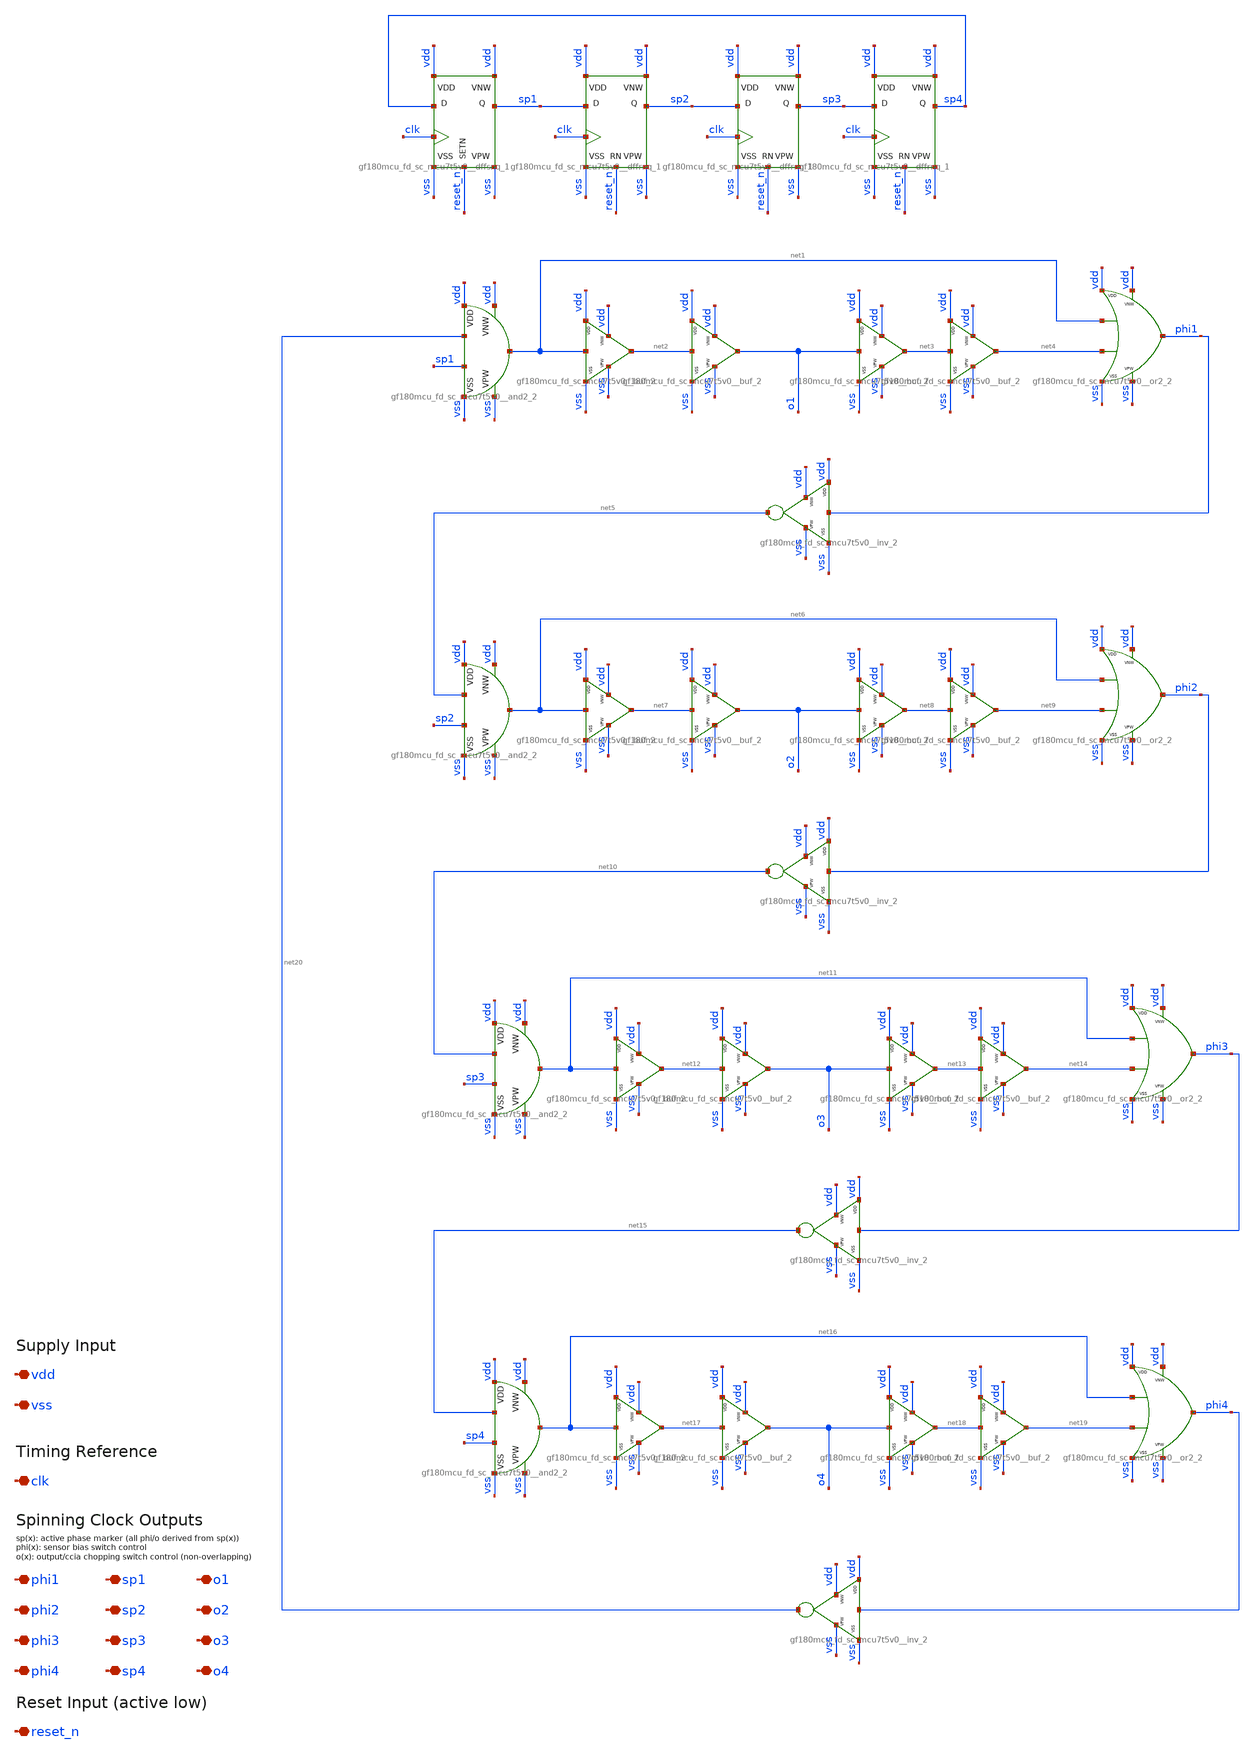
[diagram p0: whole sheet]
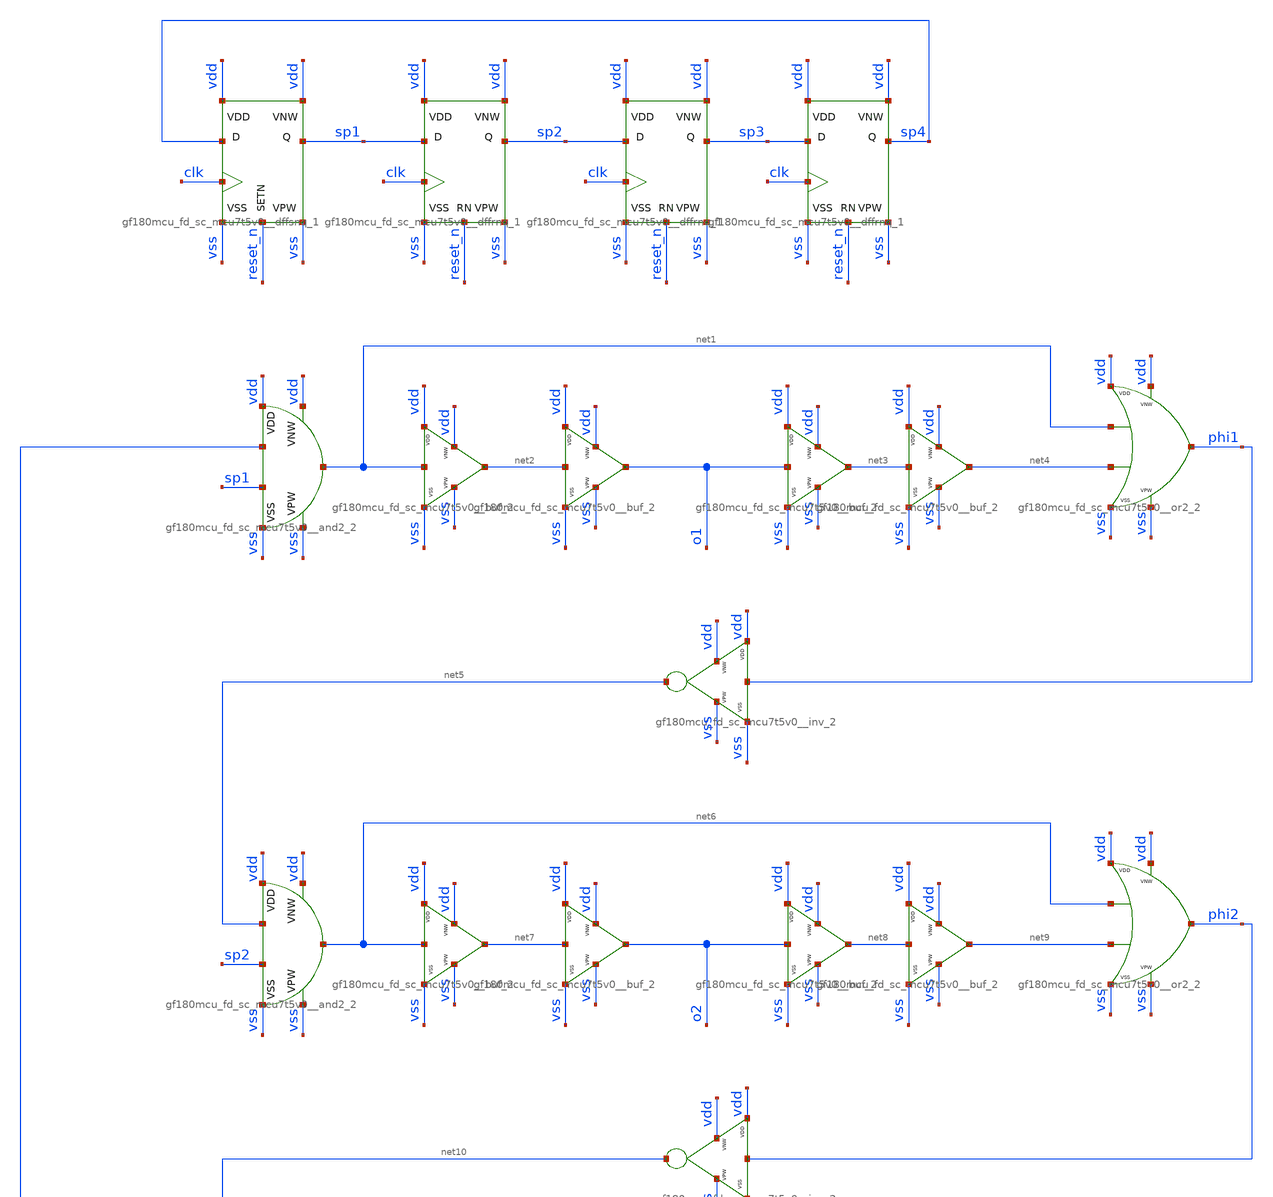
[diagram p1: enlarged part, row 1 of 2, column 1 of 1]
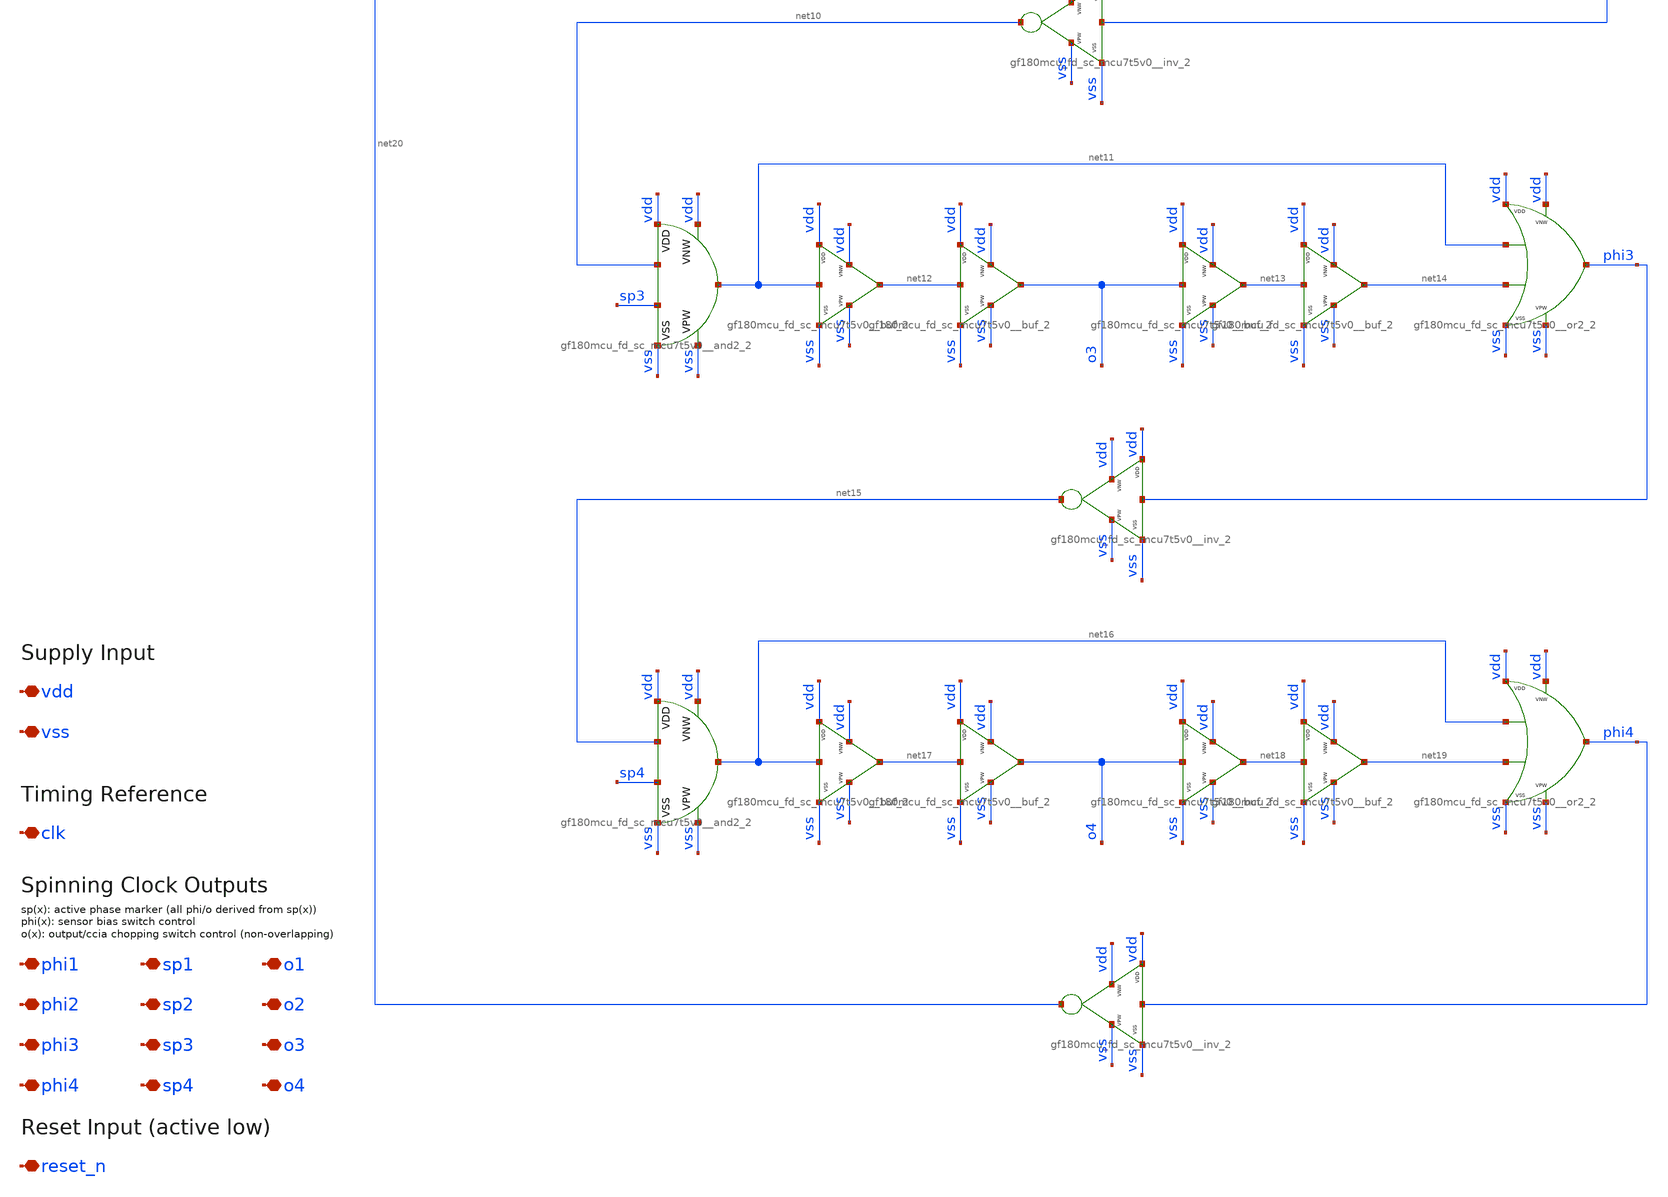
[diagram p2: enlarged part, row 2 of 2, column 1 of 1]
** sch_path: xschem/clk_gen/clk_gen.sch
**.subckt clk_gen clk phi1 phi2 phi3 phi4 sp1 sp2 sp3 sp4 o1 o2 o3 o4 vdd vss reset_n
*.iopin clk
*.iopin phi1
*.iopin phi2
*.iopin phi3
*.iopin phi4
*.iopin sp1
*.iopin sp2
*.iopin sp3
*.iopin sp4
*.iopin o1
*.iopin o2
*.iopin o3
*.iopin o4
*.iopin vdd
*.iopin vss
*.iopin reset_n
x1 sp4 reset_n clk sp1 vdd vdd vss vss gf180mcu_fd_sc_mcu7t5v0__dffsnq_1
x2 sp1 reset_n clk sp2 vdd vdd vss vss gf180mcu_fd_sc_mcu7t5v0__dffrnq_1
x3 sp2 reset_n clk sp3 vdd vdd vss vss gf180mcu_fd_sc_mcu7t5v0__dffrnq_1
x4 sp3 reset_n clk sp4 vdd vdd vss vss gf180mcu_fd_sc_mcu7t5v0__dffrnq_1
x5 net20 sp1 net1 vdd vdd vss vss gf180mcu_fd_sc_mcu7t5v0__and2_2
x6 phi1 net5 vdd vdd vss vss gf180mcu_fd_sc_mcu7t5v0__inv_2
x7 net5 sp2 net6 vdd vdd vss vss gf180mcu_fd_sc_mcu7t5v0__and2_2
x8 phi2 net10 vdd vdd vss vss gf180mcu_fd_sc_mcu7t5v0__inv_2
x9 net10 sp3 net11 vdd vdd vss vss gf180mcu_fd_sc_mcu7t5v0__and2_2
x10 phi3 net15 vdd vdd vss vss gf180mcu_fd_sc_mcu7t5v0__inv_2
x11 net15 sp4 net16 vdd vdd vss vss gf180mcu_fd_sc_mcu7t5v0__and2_2
x12 phi4 net20 vdd vdd vss vss gf180mcu_fd_sc_mcu7t5v0__inv_2
x13 net1 net2 vdd vdd vss vss gf180mcu_fd_sc_mcu7t5v0__buf_2
x14 net2 o1 vdd vdd vss vss gf180mcu_fd_sc_mcu7t5v0__buf_2
x15 o1 net3 vdd vdd vss vss gf180mcu_fd_sc_mcu7t5v0__buf_2
x16 net3 net4 vdd vdd vss vss gf180mcu_fd_sc_mcu7t5v0__buf_2
x17 net6 net7 vdd vdd vss vss gf180mcu_fd_sc_mcu7t5v0__buf_2
x18 net7 o2 vdd vdd vss vss gf180mcu_fd_sc_mcu7t5v0__buf_2
x19 o2 net8 vdd vdd vss vss gf180mcu_fd_sc_mcu7t5v0__buf_2
x20 net8 net9 vdd vdd vss vss gf180mcu_fd_sc_mcu7t5v0__buf_2
x21 net11 net12 vdd vdd vss vss gf180mcu_fd_sc_mcu7t5v0__buf_2
x22 net12 o3 vdd vdd vss vss gf180mcu_fd_sc_mcu7t5v0__buf_2
x23 o3 net13 vdd vdd vss vss gf180mcu_fd_sc_mcu7t5v0__buf_2
x24 net13 net14 vdd vdd vss vss gf180mcu_fd_sc_mcu7t5v0__buf_2
x25 net16 net17 vdd vdd vss vss gf180mcu_fd_sc_mcu7t5v0__buf_2
x26 net17 o4 vdd vdd vss vss gf180mcu_fd_sc_mcu7t5v0__buf_2
x27 o4 net18 vdd vdd vss vss gf180mcu_fd_sc_mcu7t5v0__buf_2
x28 net18 net19 vdd vdd vss vss gf180mcu_fd_sc_mcu7t5v0__buf_2
x29 net16 net19 phi4 vdd vdd vss vss gf180mcu_fd_sc_mcu7t5v0__or2_2
x30 net11 net14 phi3 vdd vdd vss vss gf180mcu_fd_sc_mcu7t5v0__or2_2
x31 net6 net9 phi2 vdd vdd vss vss gf180mcu_fd_sc_mcu7t5v0__or2_2
x32 net1 net4 phi1 vdd vdd vss vss gf180mcu_fd_sc_mcu7t5v0__or2_2
**.ends
.end
